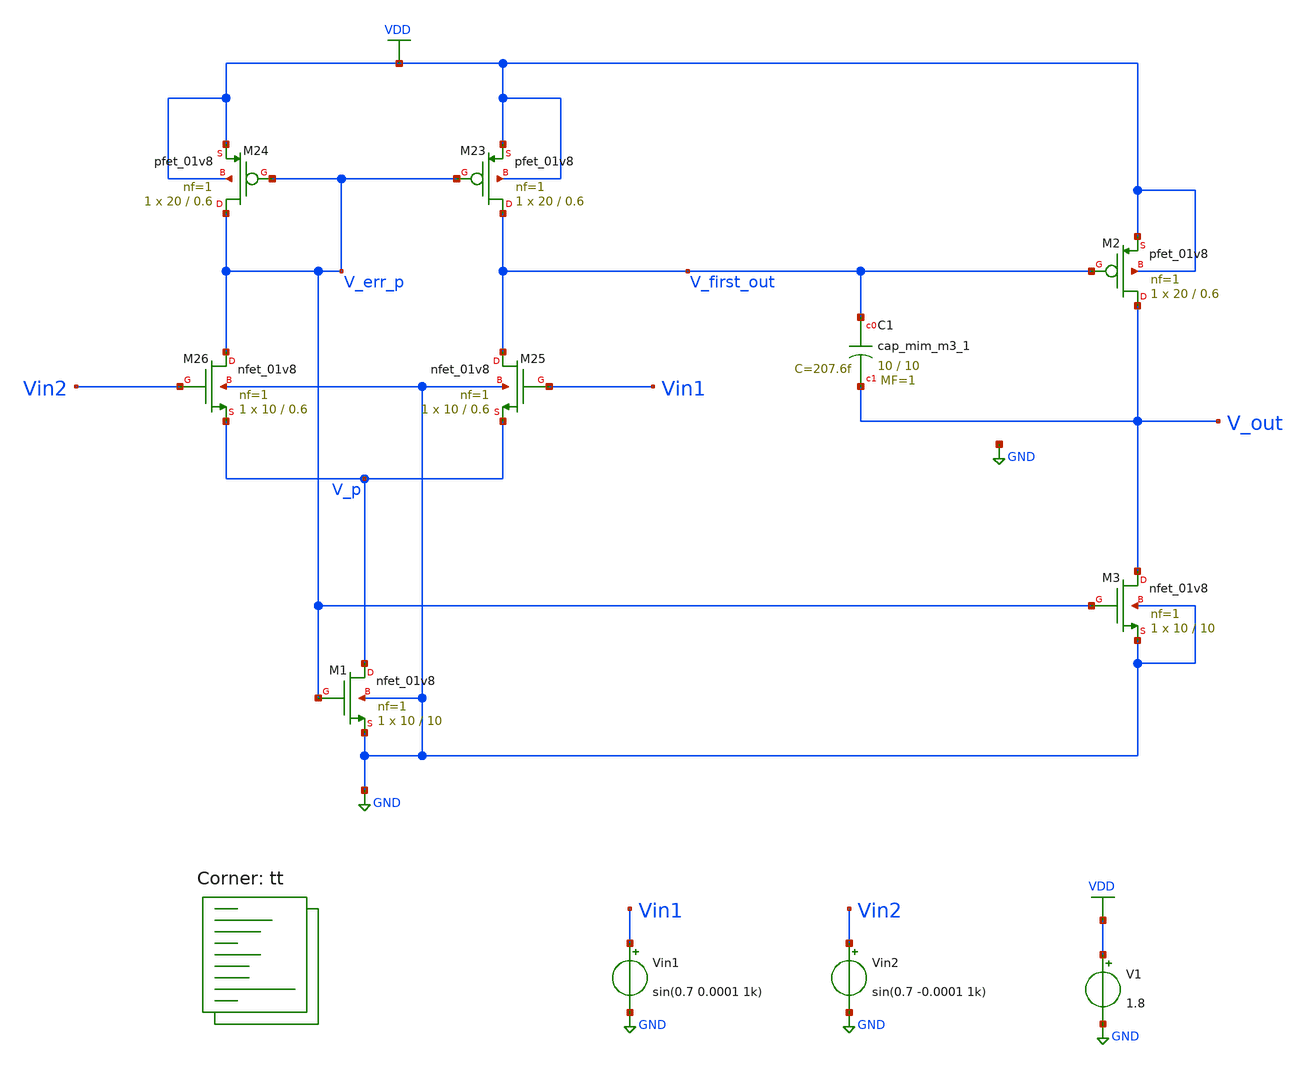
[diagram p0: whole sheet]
** sch_path: projects/bandgapref/xschem_ngspice/new_files/tb_opamp_bandgap_3.sch
**.subckt tb_opamp_bandgap_3
V1 VDD GND 1.8
Vin1 Vin1 GND sin(0.7 0.0001 1k)
Vin2 Vin2 GND sin(0.7 -0.0001 1k)
XM23 V_first_out V_err_p VDD VDD sky130_fd_pr__pfet_01v8 L=0.6 W=20 nf=1 ad='int((nf+1)/2) * W/nf * 0.29'
+ as='int((nf+2)/2) * W/nf * 0.29' pd='2*int((nf+1)/2) * (W/nf + 0.29)' ps='2*int((nf+2)/2) * (W/nf + 0.29)'
+ nrd='0.29 / W' nrs='0.29 / W' sa=0 sb=0 sd=0 mult=1 m=1
XM24 V_err_p V_err_p VDD VDD sky130_fd_pr__pfet_01v8 L=0.6 W=20 nf=1 ad='int((nf+1)/2) * W/nf * 0.29'
+ as='int((nf+2)/2) * W/nf * 0.29' pd='2*int((nf+1)/2) * (W/nf + 0.29)' ps='2*int((nf+2)/2) * (W/nf + 0.29)'
+ nrd='0.29 / W' nrs='0.29 / W' sa=0 sb=0 sd=0 mult=1 m=1
XM25 V_first_out Vin1 V_p GND sky130_fd_pr__nfet_01v8 L=0.6 W=10 nf=1 ad='int((nf+1)/2) * W/nf * 0.29'
+ as='int((nf+2)/2) * W/nf * 0.29' pd='2*int((nf+1)/2) * (W/nf + 0.29)' ps='2*int((nf+2)/2) * (W/nf + 0.29)'
+ nrd='0.29 / W' nrs='0.29 / W' sa=0 sb=0 sd=0 mult=1 m=1
XM26 V_err_p Vin2 V_p GND sky130_fd_pr__nfet_01v8 L=0.6 W=10 nf=1 ad='int((nf+1)/2) * W/nf * 0.29' as='int((nf+2)/2) * W/nf * 0.29'
+ pd='2*int((nf+1)/2) * (W/nf + 0.29)' ps='2*int((nf+2)/2) * (W/nf + 0.29)' nrd='0.29 / W' nrs='0.29 / W'
+ sa=0 sb=0 sd=0 mult=1 m=1
XM1 V_p V_err_p GND GND sky130_fd_pr__nfet_01v8 L=10 W=10 nf=1 ad='int((nf+1)/2) * W/nf * 0.29' as='int((nf+2)/2) * W/nf * 0.29'
+ pd='2*int((nf+1)/2) * (W/nf + 0.29)' ps='2*int((nf+2)/2) * (W/nf + 0.29)' nrd='0.29 / W' nrs='0.29 / W'
+ sa=0 sb=0 sd=0 mult=1 m=1
XM2 V_out V_first_out VDD VDD sky130_fd_pr__pfet_01v8 L=0.6 W=20 nf=1 ad='int((nf+1)/2) * W/nf * 0.29'
+ as='int((nf+2)/2) * W/nf * 0.29' pd='2*int((nf+1)/2) * (W/nf + 0.29)' ps='2*int((nf+2)/2) * (W/nf + 0.29)'
+ nrd='0.29 / W' nrs='0.29 / W' sa=0 sb=0 sd=0 mult=1 m=1
XM3 V_out V_err_p GND GND sky130_fd_pr__nfet_01v8 L=10 W=10 nf=1 ad='int((nf+1)/2) * W/nf * 0.29' as='int((nf+2)/2) * W/nf * 0.29'
+ pd='2*int((nf+1)/2) * (W/nf + 0.29)' ps='2*int((nf+2)/2) * (W/nf + 0.29)' nrd='0.29 / W' nrs='0.29 / W'
+ sa=0 sb=0 sd=0 mult=1 m=1
XC1 V_first_out V_out sky130_fd_pr__cap_mim_m3_1 W=10 L=10 MF=1 m=1
**** begin user architecture code



.option wnflag=1
.option savecurrents

.save @m.xm1.msky130_fd_pr__nfet_01v8[gm] @m.xm2.msky130_fd_pr__nfet_01v8[gm] @m.xm3.msky130_fd_pr__nfet_01v8[gm] @m.xm4.msky130_fd_pr__pfet_01v8[gm] @m.xm5.msky130_fd_pr__pfet_01v8[gm] @m.xm6.msky130_fd_pr__nfet_01v8[gm] @m.xm7.msky130_fd_pr__pfet_01v8[gm]

.control

  save all
  tran 1u 3m
  * ac dec 20 1 1T
  write tb_opamp_bandgap_3.raw
  set appendwrite

.endc



.lib $::SKYWATER_MODELS/sky130.lib.spice tt
**** end user architecture code
**.ends
.GLOBAL GND
.GLOBAL VDD
.end
